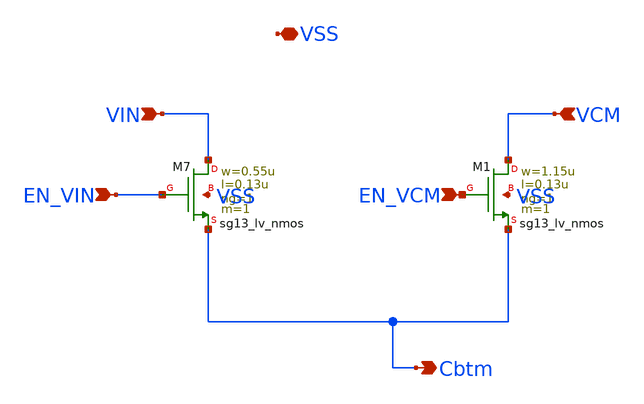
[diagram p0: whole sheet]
** sch_path: schematic/individual_switches/switch_C0_dummy.sch
**.subckt switch_C0_dummy VIN EN_VIN VCM EN_VCM Cbtm VSS
*.ipin VIN
*.ipin EN_VIN
*.ipin VCM
*.ipin EN_VCM
*.opin Cbtm
*.iopin VSS
XM7 VIN EN_VIN Cbtm VSS sg13_lv_nmos w=0.55u l=0.13u ng=1 m=1 mm_ok=1
XM1 VCM EN_VCM Cbtm VSS sg13_lv_nmos w=1.15u l=0.13u ng=1 m=1 mm_ok=1
**.ends
.end
